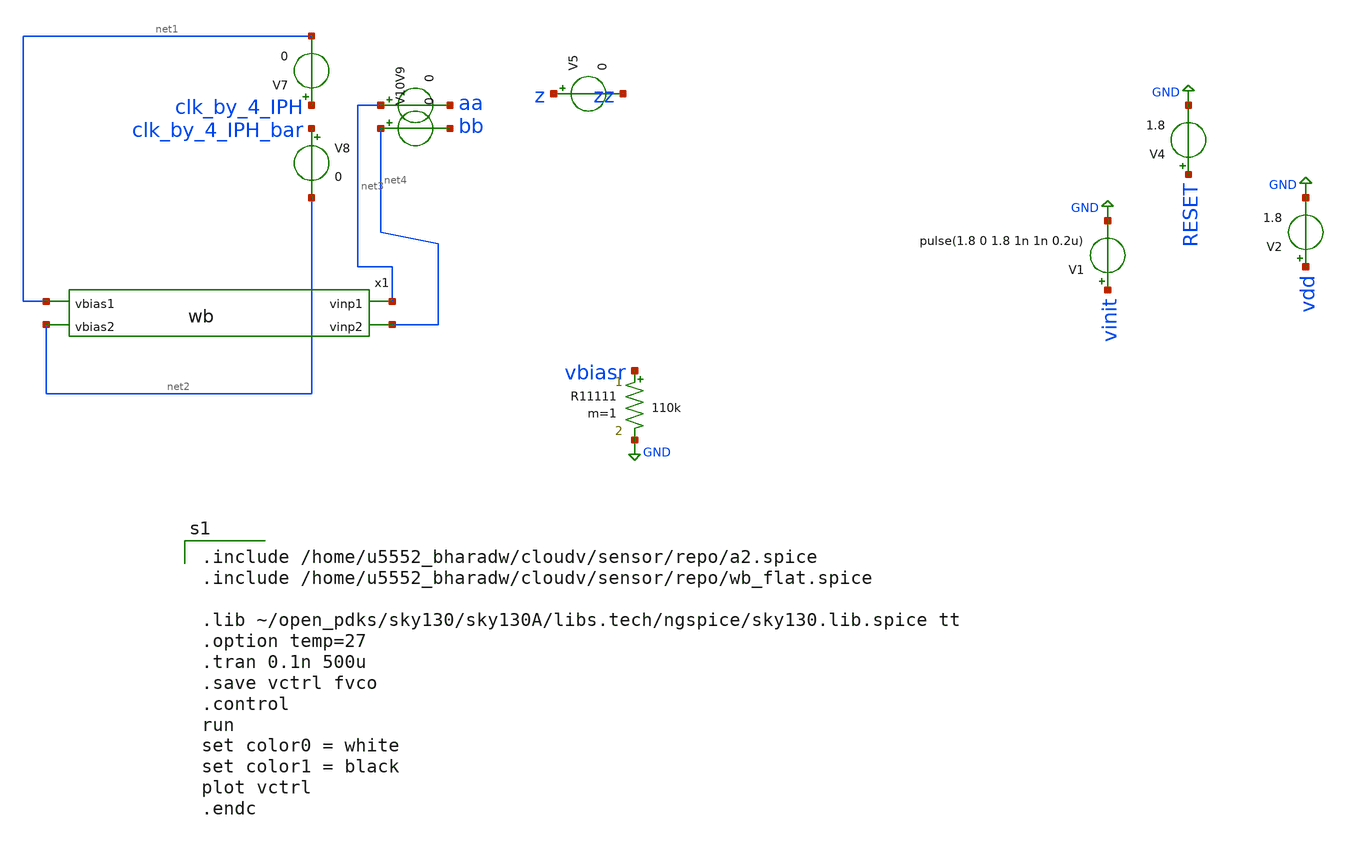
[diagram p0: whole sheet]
** sch_path: untitled-471.sch
**.subckt untitled-471
V2 vdd GND 1.8
V1 vinit GND pulse(1.8 0 1.8 1n 1n 0.2u)
V4 RESET GND 1.8
R11111 vbiasr GND 110k m=1
V5 z zz 0
V7 clk_by_4_IPH net1 0
V8 clk_by_4_IPH_bar net2 0
V9 net3 aa 0
V10 net4 bb 0
x1 net1 net3 net2 net4 wb
**** begin user architecture code

.include /home/u5552_bharadw/cloudv/sensor/repo/a2.spice
.include /home/u5552_bharadw/cloudv/sensor/repo/wb_flat.spice

.lib ~/open_pdks/sky130/sky130A/libs.tech/ngspice/sky130.lib.spice tt
.option temp=27
.tran 0.1n 500u
.save vctrl fvco
.control
run
set color0 = white
set color1 = black
plot vctrl
.endc


**** end user architecture code
**.ends
.GLOBAL GND
.end
